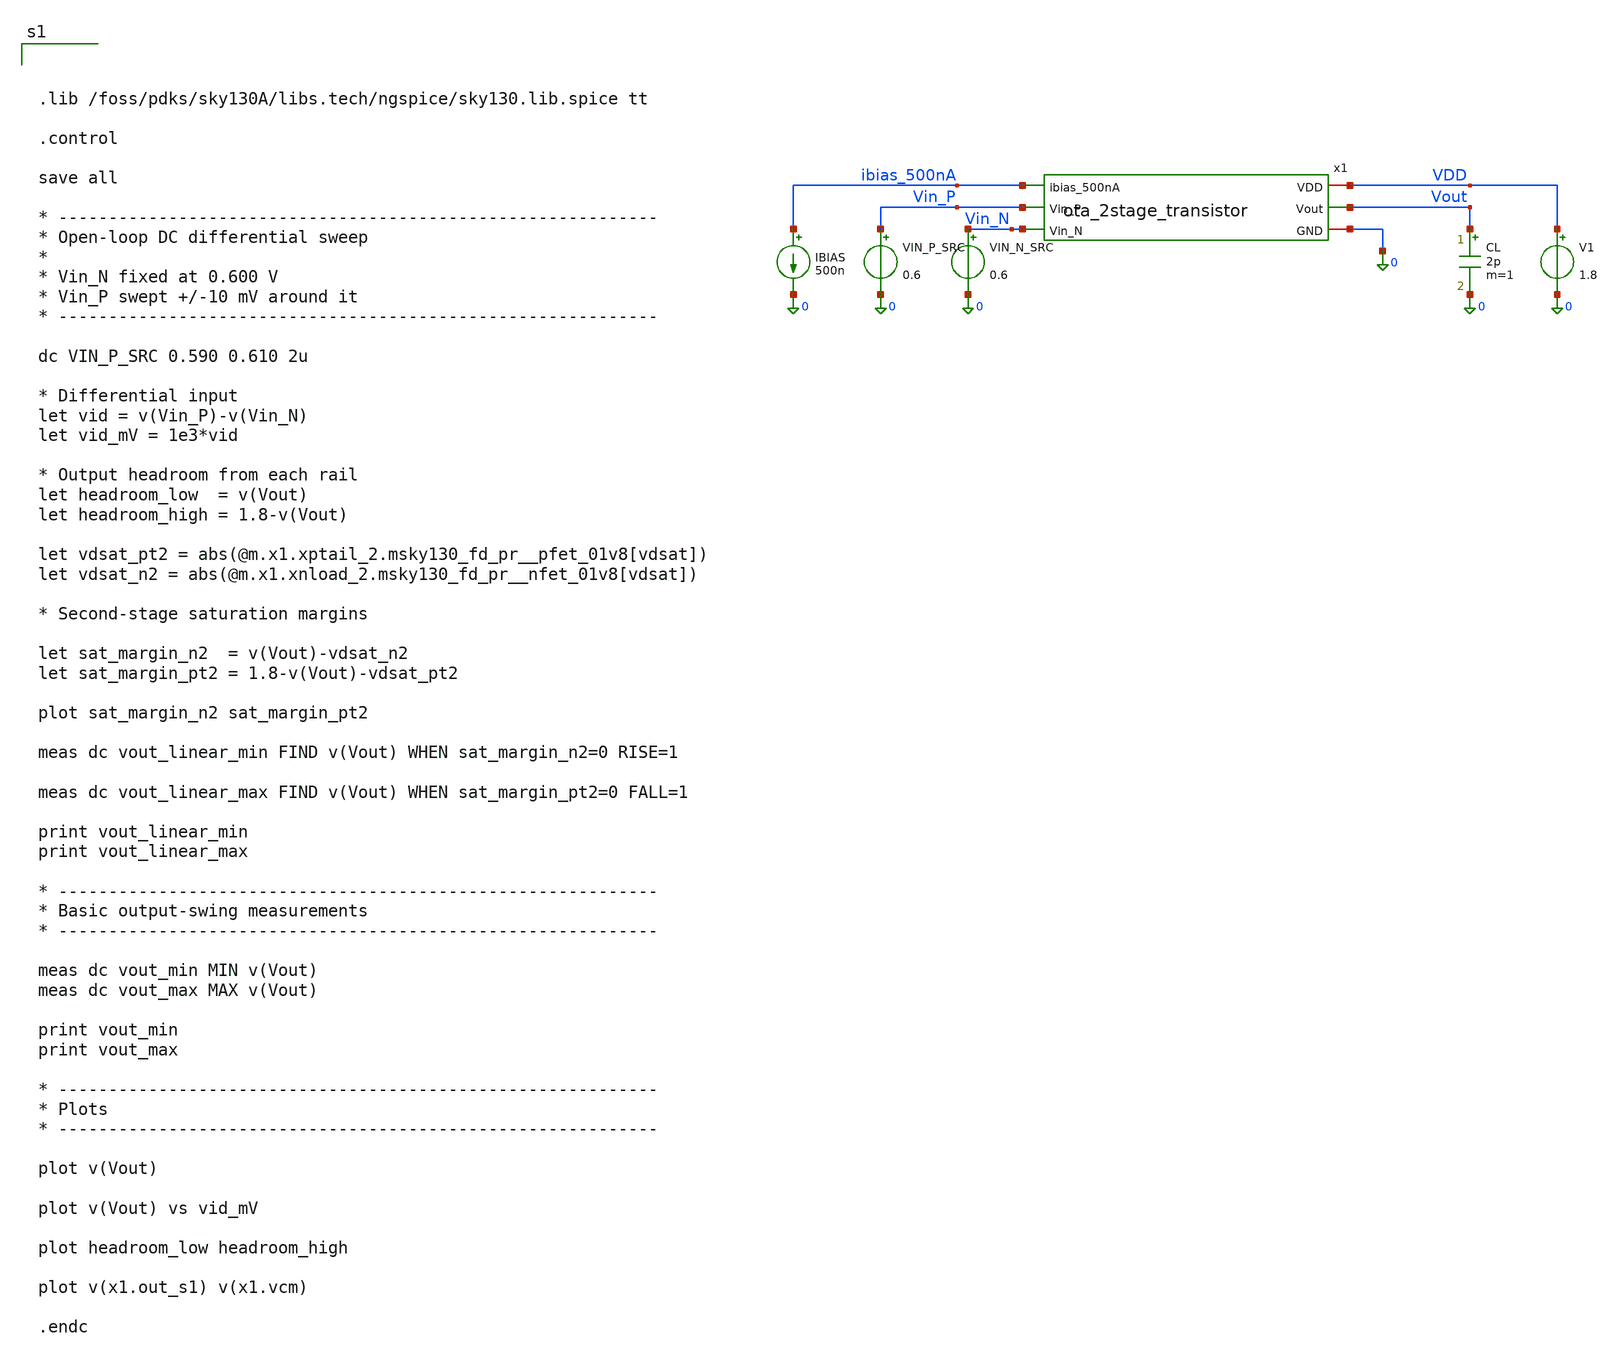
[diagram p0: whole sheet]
** sch_path: dfii/project_2stage_OTA_sim/tb_ota_2stage_output_swing.sch
**.subckt tb_ota_2stage_output_swing
x1 VDD ibias_500nA Vout Vin_P Vin_N 0 ota_2stage_transistor
V1 VDD 0 1.8
IBIAS ibias_500nA 0 500n
VIN_P_SRC Vin_P 0 0.6
CL Vout 0 2p m=1
VIN_N_SRC Vin_N 0 0.6
**** begin user architecture code



.lib /foss/pdks/sky130A/libs.tech/ngspice/sky130.lib.spice tt

.control

save all

* ------------------------------------------------------------
* Open-loop DC differential sweep
*
* Vin_N fixed at 0.600 V
* Vin_P swept +/-10 mV around it
* ------------------------------------------------------------

dc VIN_P_SRC 0.590 0.610 2u

* Differential input
let vid = v(Vin_P)-v(Vin_N)
let vid_mV = 1e3*vid

* Output headroom from each rail
let headroom_low  = v(Vout)
let headroom_high = 1.8-v(Vout)

let vdsat_pt2 = abs(@m.x1.xptail_2.msky130_fd_pr__pfet_01v8[vdsat])
let vdsat_n2 = abs(@m.x1.xnload_2.msky130_fd_pr__nfet_01v8[vdsat])

* Second-stage saturation margins

let sat_margin_n2  = v(Vout)-vdsat_n2
let sat_margin_pt2 = 1.8-v(Vout)-vdsat_pt2

plot sat_margin_n2 sat_margin_pt2

meas dc vout_linear_min FIND v(Vout) WHEN sat_margin_n2=0 RISE=1

meas dc vout_linear_max FIND v(Vout) WHEN sat_margin_pt2=0 FALL=1

print vout_linear_min
print vout_linear_max

* ------------------------------------------------------------
* Basic output-swing measurements
* ------------------------------------------------------------

meas dc vout_min MIN v(Vout)
meas dc vout_max MAX v(Vout)

print vout_min
print vout_max

* ------------------------------------------------------------
* Plots
* ------------------------------------------------------------

plot v(Vout)

plot v(Vout) vs vid_mV

plot headroom_low headroom_high

plot v(x1.out_s1) v(x1.vcm)

.endc


**** end user architecture code
**.ends

* expanding   symbol:
*+  /foss/designs/project_2stage_OTA/dfii/project_2stage_OTA/ota_2stage_transistor.sym # of pins=6
** sym_path: dfii/project_2stage_OTA/ota_2stage_transistor.sym
** sch_path: dfii/project_2stage_OTA/ota_2stage_transistor.sch
.subckt ota_2stage_transistor VDD ibias_500nA Vout Vin_P Vin_N GND
*.iopin VDD
*.iopin GND
*.ipin ibias_500nA
*.ipin Vin_N
*.ipin Vin_P
*.opin Vout
XNLOAD_0 vdiode_n vdiode_n GND GND sky130_fd_pr__nfet_01v8 L=12 W=3.6 nf=1 ad='int((1 + 1)/2) * 3.6 / 1 * 0.29'
+ as='int((1 + 2)/2) * 3.6 / 1 * 0.29' pd='2*int((1 + 1)/2) * (3.6 / 1 + 0.29)' ps='2*int((1 + 2)/2) * (3.6 / 1 + 0.29)'
+ nrd='0.29 / 3.6 ' nrs='0.29 / 3.6 ' sa=0 sb=0 sd=0 mult=1 m=1
XNLOAD_1 out_s1 vdiode_n GND GND sky130_fd_pr__nfet_01v8 L=12 W=3.6 nf=1 ad='int((1 + 1)/2) * 3.6 / 1 * 0.29'
+ as='int((1 + 2)/2) * 3.6 / 1 * 0.29' pd='2*int((1 + 1)/2) * (3.6 / 1 + 0.29)' ps='2*int((1 + 2)/2) * (3.6 / 1 + 0.29)'
+ nrd='0.29 / 3.6 ' nrs='0.29 / 3.6 ' sa=0 sb=0 sd=0 mult=1 m=1
XNLOAD_2 Vout out_s1 GND GND sky130_fd_pr__nfet_01v8 L=2 W=3.6 nf=1 ad='int((1 + 1)/2) * 3.6 / 1 * 0.29'
+ as='int((1 + 2)/2) * 3.6 / 1 * 0.29' pd='2*int((1 + 1)/2) * (3.6 / 1 + 0.29)' ps='2*int((1 + 2)/2) * (3.6 / 1 + 0.29)'
+ nrd='0.29 / 3.6 ' nrs='0.29 / 3.6 ' sa=0 sb=0 sd=0 mult=2 m=2
XPDIFF_N vdiode_n Vin_N VCM VCM sky130_fd_pr__pfet_01v8 L=1 W=7.4 nf=1 ad='int((1 + 1)/2) * 7.4 / 1 * 0.29'
+ as='int((1 + 2)/2) * 7.4 / 1 * 0.29' pd='2*int((1 + 1)/2) * (7.4 / 1 + 0.29)' ps='2*int((1 + 2)/2) * (7.4 / 1 + 0.29)'
+ nrd='0.29 / 7.4 ' nrs='0.29 / 7.4 ' sa=0 sb=0 sd=0 mult=12 m=12
XPDIFF_P out_s1 Vin_P VCM VCM sky130_fd_pr__pfet_01v8 L=1 W=7.4 nf=1 ad='int((1 + 1)/2) * 7.4 / 1 * 0.29'
+ as='int((1 + 2)/2) * 7.4 / 1 * 0.29' pd='2*int((1 + 1)/2) * (7.4 / 1 + 0.29)' ps='2*int((1 + 2)/2) * (7.4 / 1 + 0.29)'
+ nrd='0.29 / 7.4 ' nrs='0.29 / 7.4 ' sa=0 sb=0 sd=0 mult=12 m=12
XPTAIL_1 VCM ibias_500nA VDD VDD sky130_fd_pr__pfet_01v8 L=1 W=1.76 nf=1 ad='int((1 + 1)/2) * 1.76 / 1 * 0.29'
+ as='int((1 + 2)/2) * 1.76 / 1 * 0.29' pd='2*int((1 + 1)/2) * (1.76 / 1 + 0.29)' ps='2*int((1 + 2)/2) * (1.76 / 1 + 0.29)'
+ nrd='0.29 / 1.76 ' nrs='0.29 / 1.76 ' sa=0 sb=0 sd=0 mult=1 m=1
XPTAIL_2 Vout ibias_500nA VDD VDD sky130_fd_pr__pfet_01v8 L=1 W=1.76 nf=1 ad='int((1 + 1)/2) * 1.76 / 1 * 0.29'
+ as='int((1 + 2)/2) * 1.76 / 1 * 0.29' pd='2*int((1 + 1)/2) * (1.76 / 1 + 0.29)' ps='2*int((1 + 2)/2) * (1.76 / 1 + 0.29)'
+ nrd='0.29 / 1.76 ' nrs='0.29 / 1.76 ' sa=0 sb=0 sd=0 mult=6 m=6
XPTAIL_0 ibias_500nA ibias_500nA VDD VDD sky130_fd_pr__pfet_01v8 L=1 W=1.76 nf=1 ad='int((1 + 1)/2) * 1.76 / 1 * 0.29'
+ as='int((1 + 2)/2) * 1.76 / 1 * 0.29' pd='2*int((1 + 1)/2) * (1.76 / 1 + 0.29)' ps='2*int((1 + 2)/2) * (1.76 / 1 + 0.29)'
+ nrd='0.29 / 1.76 ' nrs='0.29 / 1.76 ' sa=0 sb=0 sd=0 mult=1 m=1
XCMILLER out_s1 net1 sky130_fd_pr__cap_mim_m3_1 W=19 L=19 MF=1 m=1
XRMILLER Vout net1 GND sky130_fd_pr__res_xhigh_po_0p35 L=31.5 mult=1 m=1
.ends

.GLOBAL VDD
.end
